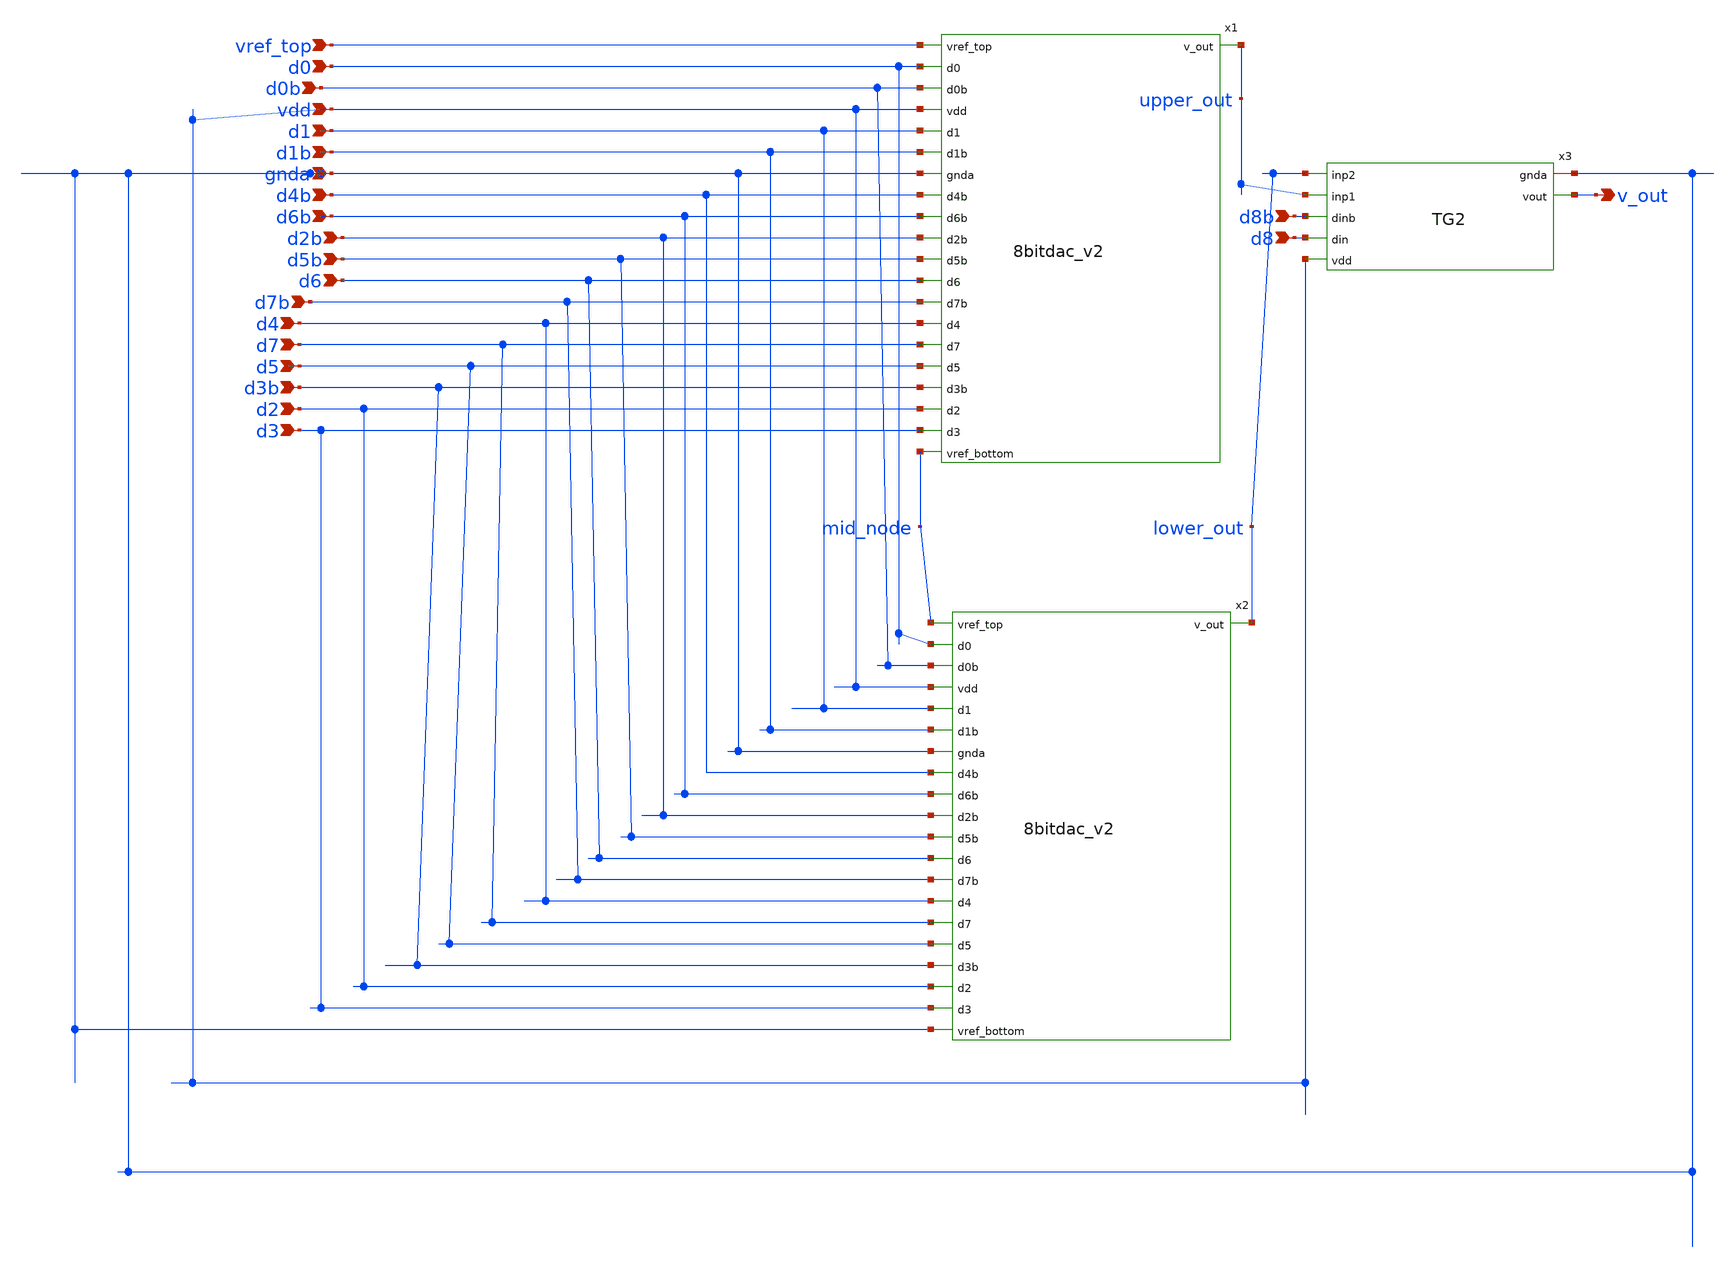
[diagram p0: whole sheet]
** sch_path: prelayout/9bitdac.sch
**.subckt 9bitdac vref_top d0 d0b vdd d1 d1b gnda d4b d6b d2b d5b d6 d7b d4 d7 d5 d3b d2 d3 d8b d8
*+ v_out
*.ipin vref_top
*.ipin d0
*.ipin d0b
*.ipin vdd
*.ipin d1
*.ipin d1b
*.ipin gnda
*.ipin d4b
*.ipin d6b
*.ipin d2b
*.ipin d5b
*.ipin d6
*.ipin d7b
*.ipin d4
*.ipin d7
*.ipin d5
*.ipin d3b
*.ipin d2
*.ipin d3
*.ipin d8b
*.ipin d8
*.opin v_out
x1 vref_top d0 d0b vdd d1 d1b gnda d4b d6b d2b d5b upper_out d6 d7b d4 d7 d5 d3b d2 d3 mid_node
+ 8bitdac_v2
x2 mid_node d0 d0b vdd d1 d1b gnda d4b d6b d2b d5b lower_out d6 d7b d4 d7 d5 d3b d2 d3 gnda
+ 8bitdac_v2
Xx3 gnda v_out lower_out upper_out d8b d8 vdd TG2
**.ends
.end
